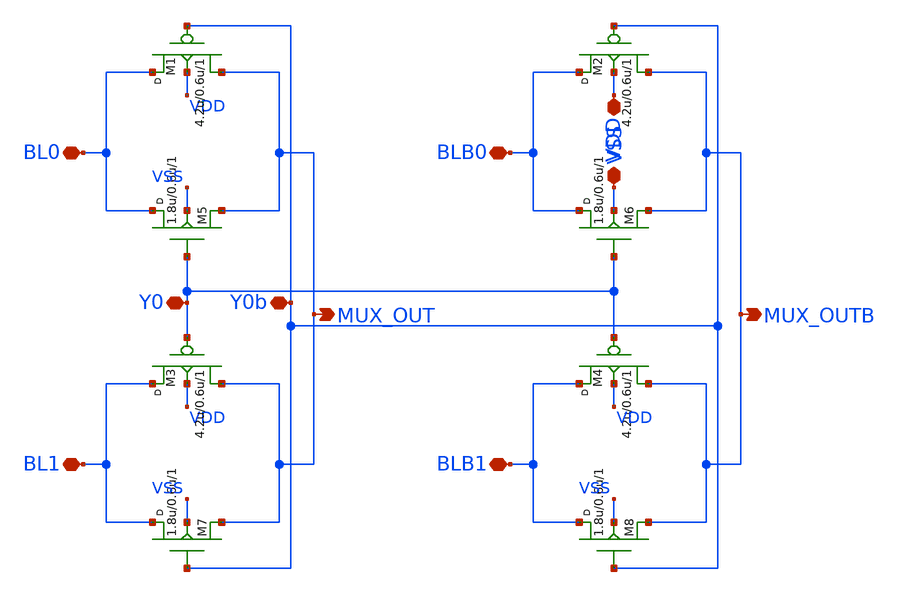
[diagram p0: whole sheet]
** sch_path: SRAM/mux/schematic/MUX1.sch
**.subckt MUX1 BL0 BLB0 BL1 BLB1 VDD VSS Y0 Y0b MUX_OUT MUX_OUTB
*.iopin BL0
*.iopin BLB0
*.iopin BL1
*.iopin BLB1
*.iopin VDD
*.iopin VSS
*.iopin Y0
*.iopin Y0b
*.opin MUX_OUT
*.opin MUX_OUTB
M1 BL0 Y0b MUX_OUT VDD pfet w=4.2u l=0.6u m=1
M2 BLB0 Y0b MUX_OUTB VDD pfet w=4.2u l=0.6u m=1
M3 BL1 Y0 MUX_OUT VDD pfet w=4.2u l=0.6u m=1
M4 BLB1 Y0 MUX_OUTB VDD pfet w=4.2u l=0.6u m=1
M5 BL0 Y0 MUX_OUT VSS nfet w=1.8u l=0.6u m=1
M6 BLB0 Y0 MUX_OUTB VSS nfet w=1.8u l=0.6u m=1
M7 BL1 Y0b MUX_OUT VSS nfet w=1.8u l=0.6u m=1
M8 BLB1 Y0b MUX_OUTB VSS nfet w=1.8u l=0.6u m=1
**.ends
.end
